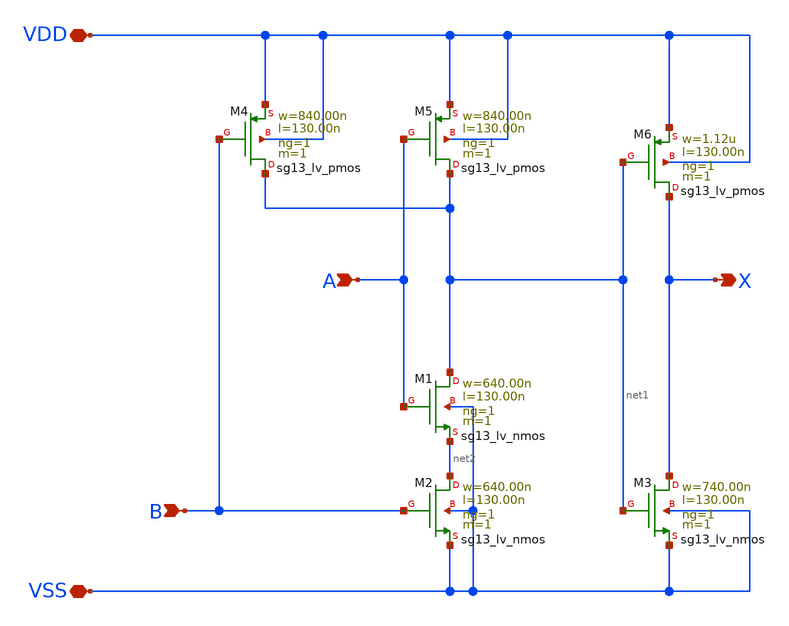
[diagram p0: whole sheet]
** sch_path: ihp-sg13g2/libs.tech/xschem/sg13g2_stdcells/sg13g2_and2_1.sch
* Copyright 2023 IHP PDK Authors
* Licensed under the Apache License, Version 2.0 (the "License");
* you may not use this file except in compliance with the License.
* You may obtain a copy of the License at
* https://www.apache.org/licenses/LICENSE-2.0
* Unless required by applicable law or agreed to in writing, software
* distributed under the License is distributed on an "AS IS" BASIS,
* WITHOUT WARRANTIES OR CONDITIONS OF ANY KIND, either express or implied.
* See the License for the specific language governing permissions and
* limitations under the License.
**.subckt sg13g2_and2_1 A B X VDD VSS
*.ipin A
*.ipin B
*.opin X
*.iopin VDD
*.iopin VSS
XM1 net1 A net2 VSS sg13_lv_nmos w=640.00n l=130.00n ng=1 m=1 mm_ok=1
XM2 net2 B VSS VSS sg13_lv_nmos w=640.00n l=130.00n ng=1 m=1 mm_ok=1
XM3 X net1 VSS VSS sg13_lv_nmos w=740.00n l=130.00n ng=1 m=1 mm_ok=1
XM4 net1 B VDD VDD sg13_lv_pmos w=840.00n l=130.00n ng=1 m=1 mm_ok=1
XM5 net1 A VDD VDD sg13_lv_pmos w=840.00n l=130.00n ng=1 m=1 mm_ok=1
XM6 X net1 VDD VDD sg13_lv_pmos w=1.12u l=130.00n ng=1 m=1 mm_ok=1
**.ends
.end
